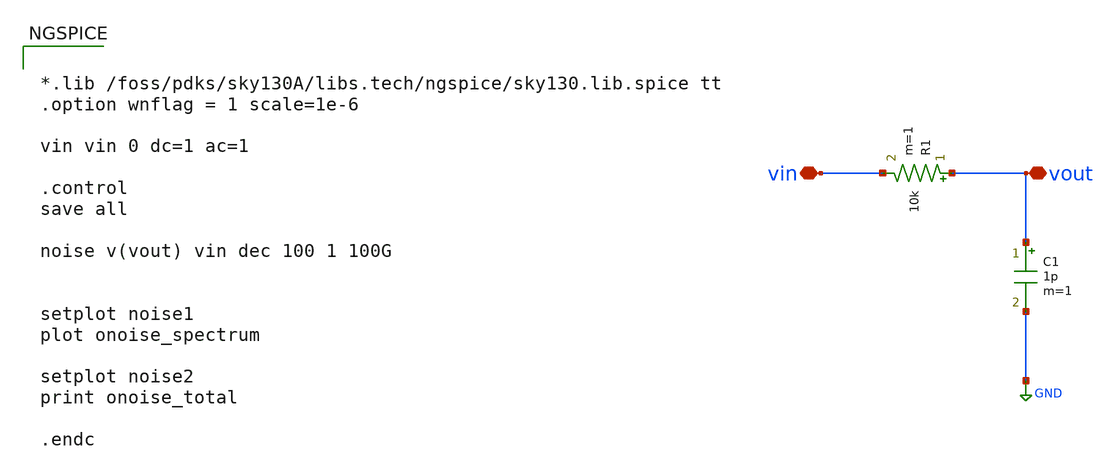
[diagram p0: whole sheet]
** sch_path: xschem/Tareas/Tarea_2/RC-noise_jm.sch
**.subckt RC-noise_jm vin vout
*.iopin vin
*.iopin vout
R1 vout vin 10k m=1
C1 vout GND 1p m=1
**** begin user architecture code


*.lib /foss/pdks/sky130A/libs.tech/ngspice/sky130.lib.spice tt
.option wnflag = 1 scale=1e-6

vin vin 0 dc=1 ac=1

.control
save all

noise v(vout) vin dec 100 1 100G


setplot noise1
plot onoise_spectrum

setplot noise2
print onoise_total

.endc


**** end user architecture code
**.ends
.GLOBAL GND
.end
